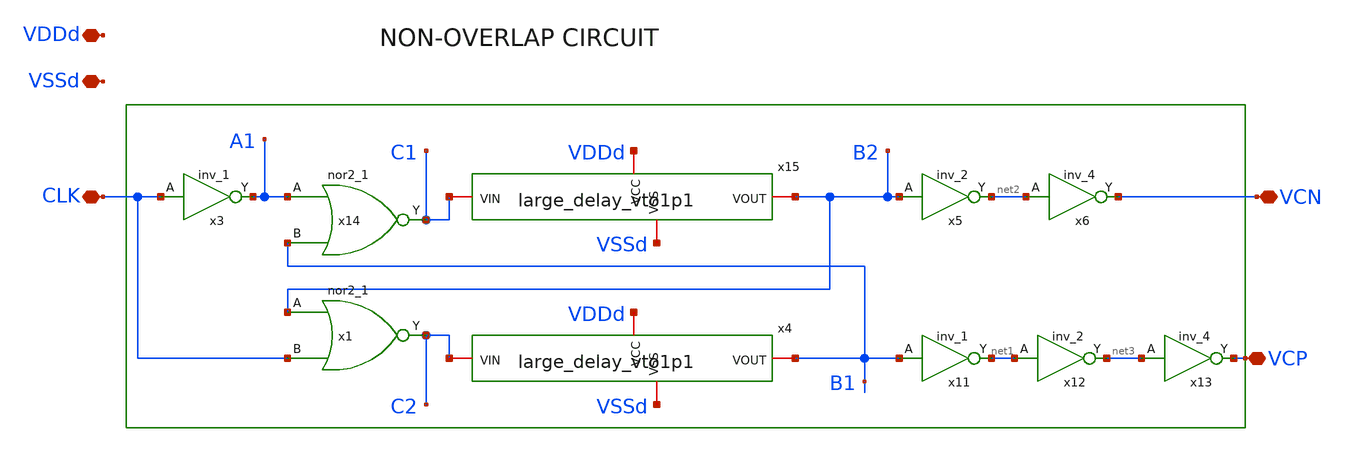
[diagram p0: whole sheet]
** sch_path: xschem/gf180_digital/NOL/NOL_vto1p1.sch
**.subckt NOL_vto1p1 CLK VCP VCN VDDd VSSd
*.iopin CLK
*.iopin VCP
*.iopin VCN
*.iopin VDDd
*.iopin VSSd
x11 B1 VSSd VDDd VSSd VDDd net1 gf180mcu_fd_sc_mcu9t5v0__inv_1
x12 net1 VSSd VDDd VSSd VDDd net3 gf180mcu_fd_sc_mcu9t5v0__inv_2
x13 net3 VSSd VDDd VSSd VDDd VCP gf180mcu_fd_sc_mcu9t5v0__inv_4
x14 A1 B1 VSSd VDDd VSSd VDDd C1 gf180mcu_fd_sc_mcu9t5v0__nor2_1
x15 VDDd VSSd C1 B2 large_delay_vto1p1
x4 VDDd VSSd C2 B1 large_delay_vto1p1
x1 B2 CLK VSSd VDDd VSSd VDDd C2 gf180mcu_fd_sc_mcu9t5v0__nor2_1
x3 CLK VSSd VDDd VSSd VDDd A1 gf180mcu_fd_sc_mcu9t5v0__inv_1
x5 B2 VSSd VDDd VSSd VDDd net2 gf180mcu_fd_sc_mcu9t5v0__inv_2
x6 net2 VSSd VDDd VSSd VDDd VCN gf180mcu_fd_sc_mcu9t5v0__inv_4
**.ends

* expanding   symbol:  gf180_digital/large_delay/large_delay_vto1p1.sym # of pins=4
** sym_path: xschem/gf180_digital/large_delay/large_delay_vto1p1.sym
** sch_path: xschem/gf180_digital/large_delay/large_delay_vto1p1.sch
.subckt large_delay_vto1p1 VDDd VSSd VIN VOUT
*.iopin VIN
*.iopin VOUT
*.iopin VDDd
*.iopin VSSd
x1 VIN VOUT VDDd VDDd VSSd VSSd gf180mcu_fd_sc_mcu9t5v0__dlya_1
.ends

.end
